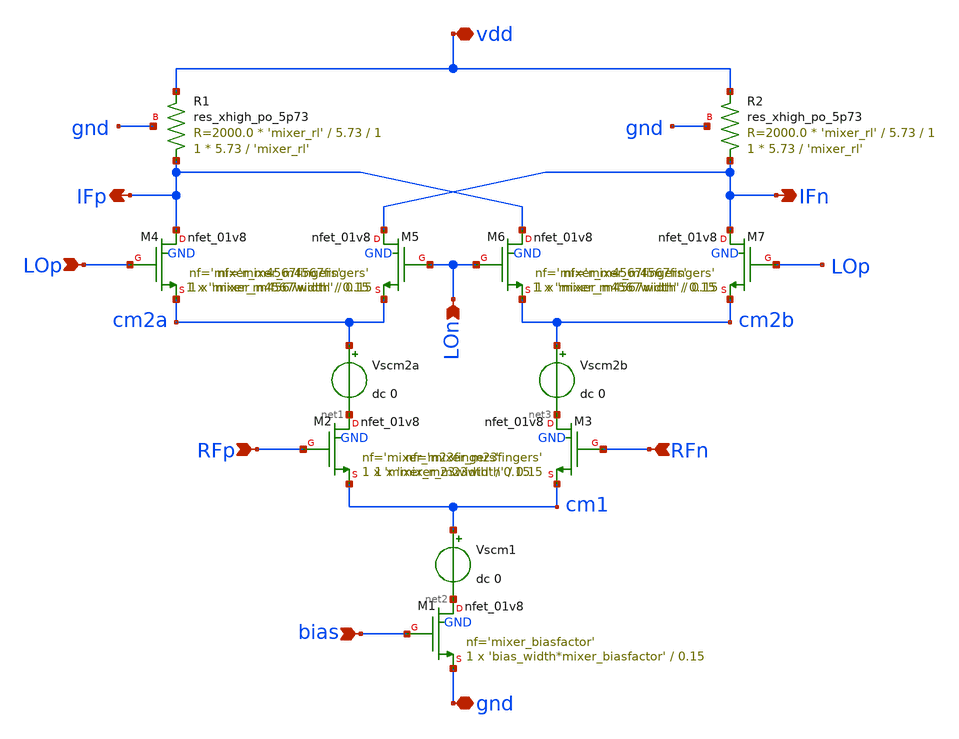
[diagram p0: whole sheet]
** sch_path: xschem/mixer_param.sch
**.subckt mixer_param LOp RFp RFn LOn bias gnd vdd IFp IFn
*.ipin LOp
*.ipin RFp
*.ipin RFn
*.ipin LOn
*.ipin bias
*.iopin gnd
*.iopin vdd
*.opin IFp
*.opin IFn
XM2 net1 RFp cm1 GND sky130_fd_pr__nfet_01v8 L=0.15 W='mixer_m23width' nf='mixer_m23fingers' ad='int((nf+1)/2) * W/nf * 0.29'
+ as='int((nf+2)/2) * W/nf * 0.29' pd='2*int((nf+1)/2) * (W/nf + 0.29)' ps='2*int((nf+2)/2) * (W/nf + 0.29)'
+ nrd='0.29 / W' nrs='0.29 / W' sa=0 sb=0 sd=0 mult=1 m=1
XM1 net2 bias gnd GND sky130_fd_pr__nfet_01v8 L=0.15 W='bias_width*mixer_biasfactor' nf='mixer_biasfactor'
+ ad='int((nf+1)/2) * W/nf * 0.29' as='int((nf+2)/2) * W/nf * 0.29' pd='2*int((nf+1)/2) * (W/nf + 0.29)'
+ ps='2*int((nf+2)/2) * (W/nf + 0.29)' nrd='0.29 / W' nrs='0.29 / W' sa=0 sb=0 sd=0 mult=1 m=1
XM3 net3 RFn cm1 GND sky130_fd_pr__nfet_01v8 L=0.15 W='mixer_m23width' nf='mixer_m23fingers' ad='int((nf+1)/2) * W/nf * 0.29'
+ as='int((nf+2)/2) * W/nf * 0.29' pd='2*int((nf+1)/2) * (W/nf + 0.29)' ps='2*int((nf+2)/2) * (W/nf + 0.29)'
+ nrd='0.29 / W' nrs='0.29 / W' sa=0 sb=0 sd=0 mult=1 m=1
XM4 IFp LOp cm2a GND sky130_fd_pr__nfet_01v8 L=0.15 W='mixer_m4567width' nf='mixer_m4567fingers' ad='int((nf+1)/2) * W/nf * 0.29'
+ as='int((nf+2)/2) * W/nf * 0.29' pd='2*int((nf+1)/2) * (W/nf + 0.29)' ps='2*int((nf+2)/2) * (W/nf + 0.29)'
+ nrd='0.29 / W' nrs='0.29 / W' sa=0 sb=0 sd=0 mult=1 m=1
XM5 IFn LOn cm2a GND sky130_fd_pr__nfet_01v8 L=0.15 W='mixer_m4567width' nf='mixer_m4567fingers' ad='int((nf+1)/2) * W/nf * 0.29'
+ as='int((nf+2)/2) * W/nf * 0.29' pd='2*int((nf+1)/2) * (W/nf + 0.29)' ps='2*int((nf+2)/2) * (W/nf + 0.29)'
+ nrd='0.29 / W' nrs='0.29 / W' sa=0 sb=0 sd=0 mult=1 m=1
XM6 IFp LOn cm2b GND sky130_fd_pr__nfet_01v8 L=0.15 W='mixer_m4567width' nf='mixer_m4567fingers' ad='int((nf+1)/2) * W/nf * 0.29'
+ as='int((nf+2)/2) * W/nf * 0.29' pd='2*int((nf+1)/2) * (W/nf + 0.29)' ps='2*int((nf+2)/2) * (W/nf + 0.29)'
+ nrd='0.29 / W' nrs='0.29 / W' sa=0 sb=0 sd=0 mult=1 m=1
XM7 IFn LOp cm2b GND sky130_fd_pr__nfet_01v8 L=0.15 W='mixer_m4567width' nf='mixer_m4567fingers' ad='int((nf+1)/2) * W/nf * 0.29'
+ as='int((nf+2)/2) * W/nf * 0.29' pd='2*int((nf+1)/2) * (W/nf + 0.29)' ps='2*int((nf+2)/2) * (W/nf + 0.29)'
+ nrd='0.29 / W' nrs='0.29 / W' sa=0 sb=0 sd=0 mult=1 m=1
Vscm1 cm1 net2 dc 0
Vscm2b cm2b net3 dc 0
Vscm2a cm2a net1 dc 0
XR1 IFp vdd gnd sky130_fd_pr__res_xhigh_po_5p73 L='mixer_rl' mult=1 m=1
XR2 IFn vdd gnd sky130_fd_pr__res_xhigh_po_5p73 L='mixer_rl' mult=1 m=1
**.ends
.end
